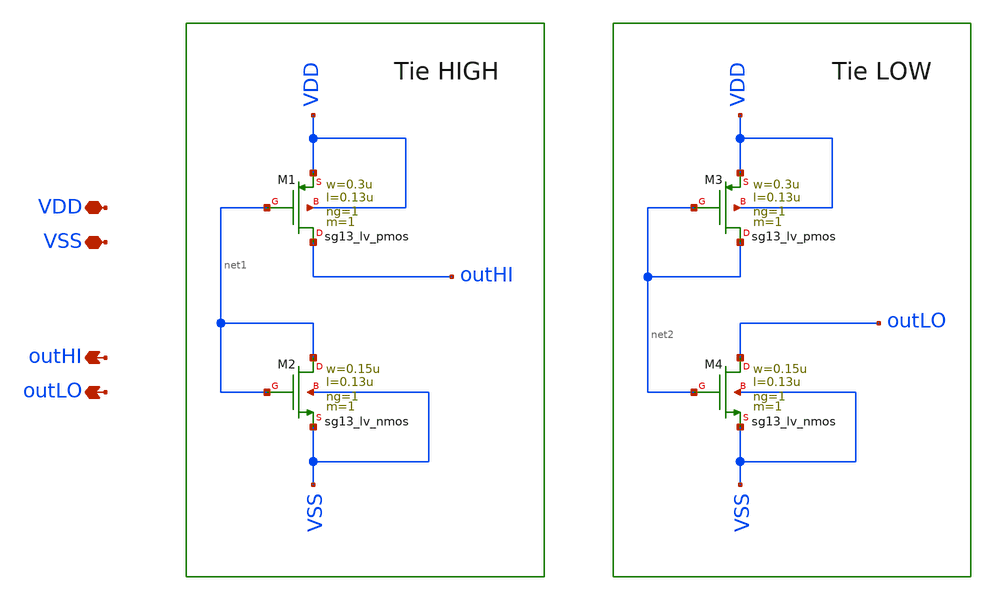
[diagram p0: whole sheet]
** sch_path: Team 2 Design/design_data/xschem/t2_tie.sch
**.subckt t2_tie VSS outLO VDD outHI
*.iopin VSS
*.opin outLO
*.iopin VDD
*.opin outHI
XM1 outHI net1 VDD VDD sg13_lv_pmos w=0.3u l=0.13u ng=1 m=1 mm_ok=1
XM2 net1 net1 VSS VSS sg13_lv_nmos w=0.15u l=0.13u ng=1 m=1 mm_ok=1
XM3 net2 net2 VDD VDD sg13_lv_pmos w=0.3u l=0.13u ng=1 m=1 mm_ok=1
XM4 outLO net2 VSS VSS sg13_lv_nmos w=0.15u l=0.13u ng=1 m=1 mm_ok=1
**.ends
.end
